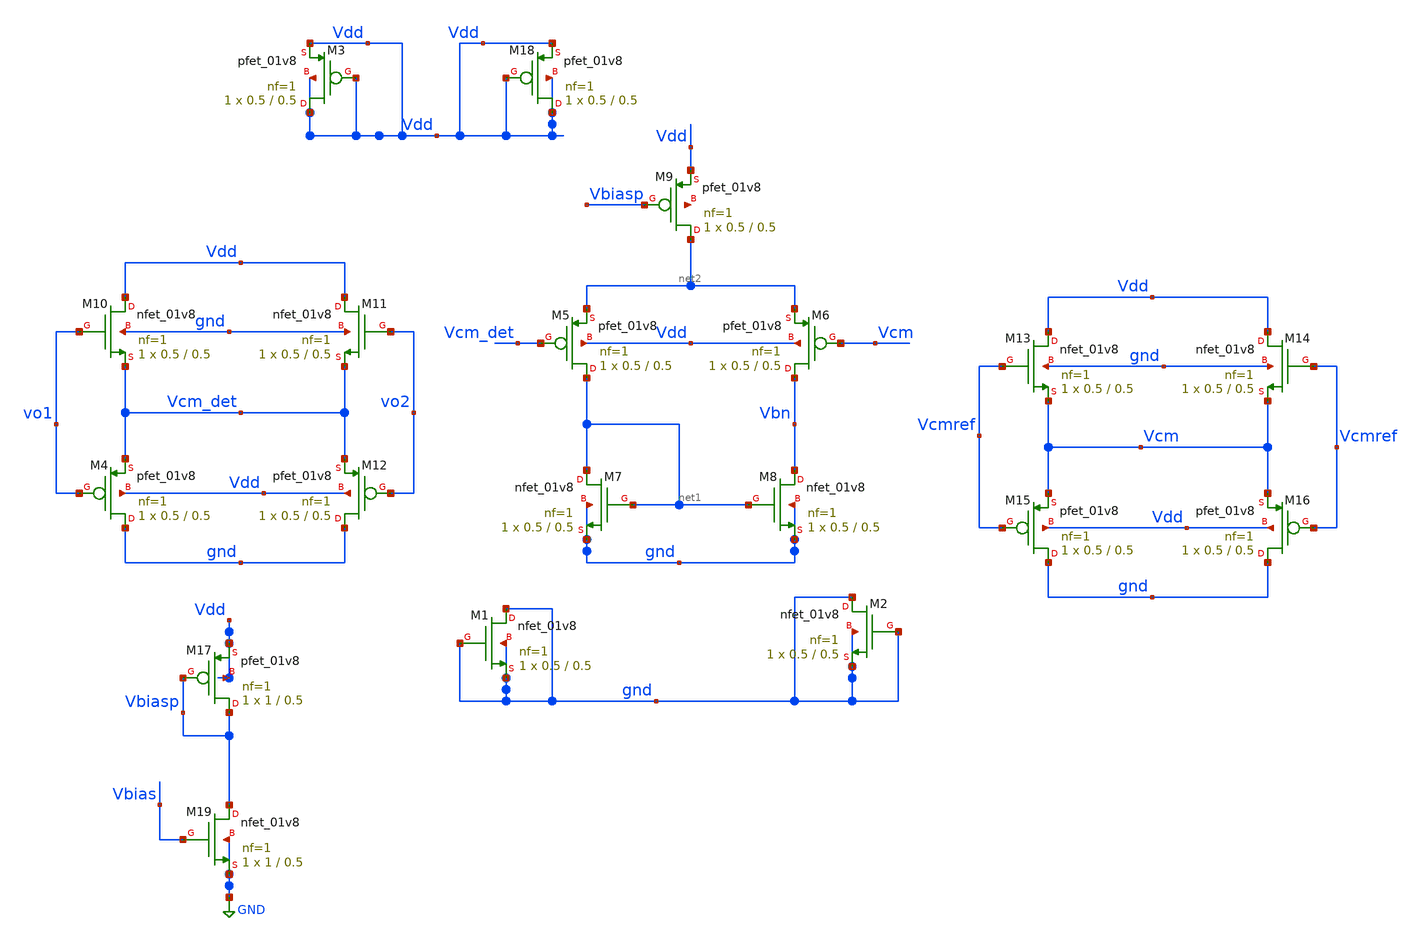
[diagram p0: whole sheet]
** sch_path: xschem/xschemfiles/cmfb_pmos_lvs.sch
**.subckt cmfb_pmos_lvs
XM4 gnd vo1 Vcm_det Vdd sky130_fd_pr__pfet_01v8 L=0.5 W=0.5 nf=1 ad='int((nf+1)/2) * W/nf * 0.29' as='int((nf+2)/2) * W/nf * 0.29'
+ pd='2*int((nf+1)/2) * (W/nf + 0.29)' ps='2*int((nf+2)/2) * (W/nf + 0.29)' nrd='0.29 / W' nrs='0.29 / W'
+ sa=0 sb=0 sd=0 mult=1 m=1
XM12 gnd vo2 Vcm_det Vdd sky130_fd_pr__pfet_01v8 L=0.5 W=0.5 nf=1 ad='int((nf+1)/2) * W/nf * 0.29' as='int((nf+2)/2) * W/nf * 0.29'
+ pd='2*int((nf+1)/2) * (W/nf + 0.29)' ps='2*int((nf+2)/2) * (W/nf + 0.29)' nrd='0.29 / W' nrs='0.29 / W'
+ sa=0 sb=0 sd=0 mult=1 m=1
XM10 Vdd vo1 Vcm_det gnd sky130_fd_pr__nfet_01v8 L=0.5 W=0.5 nf=1 ad='int((nf+1)/2) * W/nf * 0.29' as='int((nf+2)/2) * W/nf * 0.29'
+ pd='2*int((nf+1)/2) * (W/nf + 0.29)' ps='2*int((nf+2)/2) * (W/nf + 0.29)' nrd='0.29 / W' nrs='0.29 / W'
+ sa=0 sb=0 sd=0 mult=1 m=1
XM11 Vdd vo2 Vcm_det gnd sky130_fd_pr__nfet_01v8 L=0.5 W=0.5 nf=1 ad='int((nf+1)/2) * W/nf * 0.29' as='int((nf+2)/2) * W/nf * 0.29'
+ pd='2*int((nf+1)/2) * (W/nf + 0.29)' ps='2*int((nf+2)/2) * (W/nf + 0.29)' nrd='0.29 / W' nrs='0.29 / W'
+ sa=0 sb=0 sd=0 mult=1 m=1
XM5 net1 Vcm_det net2 Vdd sky130_fd_pr__pfet_01v8 L=0.5 W=0.5 nf=1 ad='int((nf+1)/2) * W/nf * 0.29' as='int((nf+2)/2) * W/nf * 0.29'
+ pd='2*int((nf+1)/2) * (W/nf + 0.29)' ps='2*int((nf+2)/2) * (W/nf + 0.29)' nrd='0.29 / W' nrs='0.29 / W'
+ sa=0 sb=0 sd=0 mult=1 m=1
XM6 Vbn Vcm net2 Vdd sky130_fd_pr__pfet_01v8 L=0.5 W=0.5 nf=1 ad='int((nf+1)/2) * W/nf * 0.29' as='int((nf+2)/2) * W/nf * 0.29'
+ pd='2*int((nf+1)/2) * (W/nf + 0.29)' ps='2*int((nf+2)/2) * (W/nf + 0.29)' nrd='0.29 / W' nrs='0.29 / W'
+ sa=0 sb=0 sd=0 mult=1 m=1
XM7 net1 net1 gnd gnd sky130_fd_pr__nfet_01v8 L=0.5 W=0.5 nf=1 ad='int((nf+1)/2) * W/nf * 0.29' as='int((nf+2)/2) * W/nf * 0.29'
+ pd='2*int((nf+1)/2) * (W/nf + 0.29)' ps='2*int((nf+2)/2) * (W/nf + 0.29)' nrd='0.29 / W' nrs='0.29 / W'
+ sa=0 sb=0 sd=0 mult=1 m=1
XM8 Vbn net1 gnd gnd sky130_fd_pr__nfet_01v8 L=0.5 W=0.5 nf=1 ad='int((nf+1)/2) * W/nf * 0.29' as='int((nf+2)/2) * W/nf * 0.29'
+ pd='2*int((nf+1)/2) * (W/nf + 0.29)' ps='2*int((nf+2)/2) * (W/nf + 0.29)' nrd='0.29 / W' nrs='0.29 / W'
+ sa=0 sb=0 sd=0 mult=1 m=1
XM13 Vdd Vcmref Vcm gnd sky130_fd_pr__nfet_01v8 L=0.5 W=0.5 nf=1 ad='int((nf+1)/2) * W/nf * 0.29' as='int((nf+2)/2) * W/nf * 0.29'
+ pd='2*int((nf+1)/2) * (W/nf + 0.29)' ps='2*int((nf+2)/2) * (W/nf + 0.29)' nrd='0.29 / W' nrs='0.29 / W'
+ sa=0 sb=0 sd=0 mult=1 m=1
XM14 Vdd Vcmref Vcm gnd sky130_fd_pr__nfet_01v8 L=0.5 W=0.5 nf=1 ad='int((nf+1)/2) * W/nf * 0.29' as='int((nf+2)/2) * W/nf * 0.29'
+ pd='2*int((nf+1)/2) * (W/nf + 0.29)' ps='2*int((nf+2)/2) * (W/nf + 0.29)' nrd='0.29 / W' nrs='0.29 / W'
+ sa=0 sb=0 sd=0 mult=1 m=1
XM15 gnd Vcmref Vcm Vdd sky130_fd_pr__pfet_01v8 L=0.5 W=0.5 nf=1 ad='int((nf+1)/2) * W/nf * 0.29' as='int((nf+2)/2) * W/nf * 0.29'
+ pd='2*int((nf+1)/2) * (W/nf + 0.29)' ps='2*int((nf+2)/2) * (W/nf + 0.29)' nrd='0.29 / W' nrs='0.29 / W'
+ sa=0 sb=0 sd=0 mult=1 m=1
XM16 gnd Vcmref Vcm Vdd sky130_fd_pr__pfet_01v8 L=0.5 W=0.5 nf=1 ad='int((nf+1)/2) * W/nf * 0.29' as='int((nf+2)/2) * W/nf * 0.29'
+ pd='2*int((nf+1)/2) * (W/nf + 0.29)' ps='2*int((nf+2)/2) * (W/nf + 0.29)' nrd='0.29 / W' nrs='0.29 / W'
+ sa=0 sb=0 sd=0 mult=1 m=1
XM1 gnd gnd gnd gnd sky130_fd_pr__nfet_01v8 L=0.5 W=0.5 nf=1 ad='int((nf+1)/2) * W/nf * 0.29' as='int((nf+2)/2) * W/nf * 0.29'
+ pd='2*int((nf+1)/2) * (W/nf + 0.29)' ps='2*int((nf+2)/2) * (W/nf + 0.29)' nrd='0.29 / W' nrs='0.29 / W'
+ sa=0 sb=0 sd=0 mult=1 m=1
XM2 gnd gnd gnd gnd sky130_fd_pr__nfet_01v8 L=0.5 W=0.5 nf=1 ad='int((nf+1)/2) * W/nf * 0.29' as='int((nf+2)/2) * W/nf * 0.29'
+ pd='2*int((nf+1)/2) * (W/nf + 0.29)' ps='2*int((nf+2)/2) * (W/nf + 0.29)' nrd='0.29 / W' nrs='0.29 / W'
+ sa=0 sb=0 sd=0 mult=1 m=1
XM3 Vdd Vdd Vdd Vdd sky130_fd_pr__pfet_01v8 L=0.5 W=0.5 nf=1 ad='int((nf+1)/2) * W/nf * 0.29' as='int((nf+2)/2) * W/nf * 0.29'
+ pd='2*int((nf+1)/2) * (W/nf + 0.29)' ps='2*int((nf+2)/2) * (W/nf + 0.29)' nrd='0.29 / W' nrs='0.29 / W'
+ sa=0 sb=0 sd=0 mult=1 m=1
XM18 Vdd Vdd Vdd Vdd sky130_fd_pr__pfet_01v8 L=0.5 W=0.5 nf=1 ad='int((nf+1)/2) * W/nf * 0.29' as='int((nf+2)/2) * W/nf * 0.29'
+ pd='2*int((nf+1)/2) * (W/nf + 0.29)' ps='2*int((nf+2)/2) * (W/nf + 0.29)' nrd='0.29 / W' nrs='0.29 / W'
+ sa=0 sb=0 sd=0 mult=1 m=1
XM9 net2 Vbiasp Vdd net3 sky130_fd_pr__pfet_01v8 L=0.5 W=0.5 nf=1 ad='int((nf+1)/2) * W/nf * 0.29' as='int((nf+2)/2) * W/nf * 0.29'
+ pd='2*int((nf+1)/2) * (W/nf + 0.29)' ps='2*int((nf+2)/2) * (W/nf + 0.29)' nrd='0.29 / W' nrs='0.29 / W'
+ sa=0 sb=0 sd=0 mult=1 m=1
XM17 Vbiasp Vbiasp Vdd Vdd sky130_fd_pr__pfet_01v8 L=0.5 W=1 nf=1 ad='int((nf+1)/2) * W/nf * 0.29' as='int((nf+2)/2) * W/nf * 0.29'
+ pd='2*int((nf+1)/2) * (W/nf + 0.29)' ps='2*int((nf+2)/2) * (W/nf + 0.29)' nrd='0.29 / W' nrs='0.29 / W'
+ sa=0 sb=0 sd=0 mult=1 m=1
XM19 Vbiasp Vbias GND GND sky130_fd_pr__nfet_01v8 L=0.5 W=1 nf=1 ad='int((nf+1)/2) * W/nf * 0.29' as='int((nf+2)/2) * W/nf * 0.29'
+ pd='2*int((nf+1)/2) * (W/nf + 0.29)' ps='2*int((nf+2)/2) * (W/nf + 0.29)' nrd='0.29 / W' nrs='0.29 / W'
+ sa=0 sb=0 sd=0 mult=1 m=1
**** begin user architecture code

** opencircuitdesign pdks install
.lib $::SKYWATER_MODELS/sky130.lib.spice tt


**** end user architecture code
**.ends
.GLOBAL GND
.end
